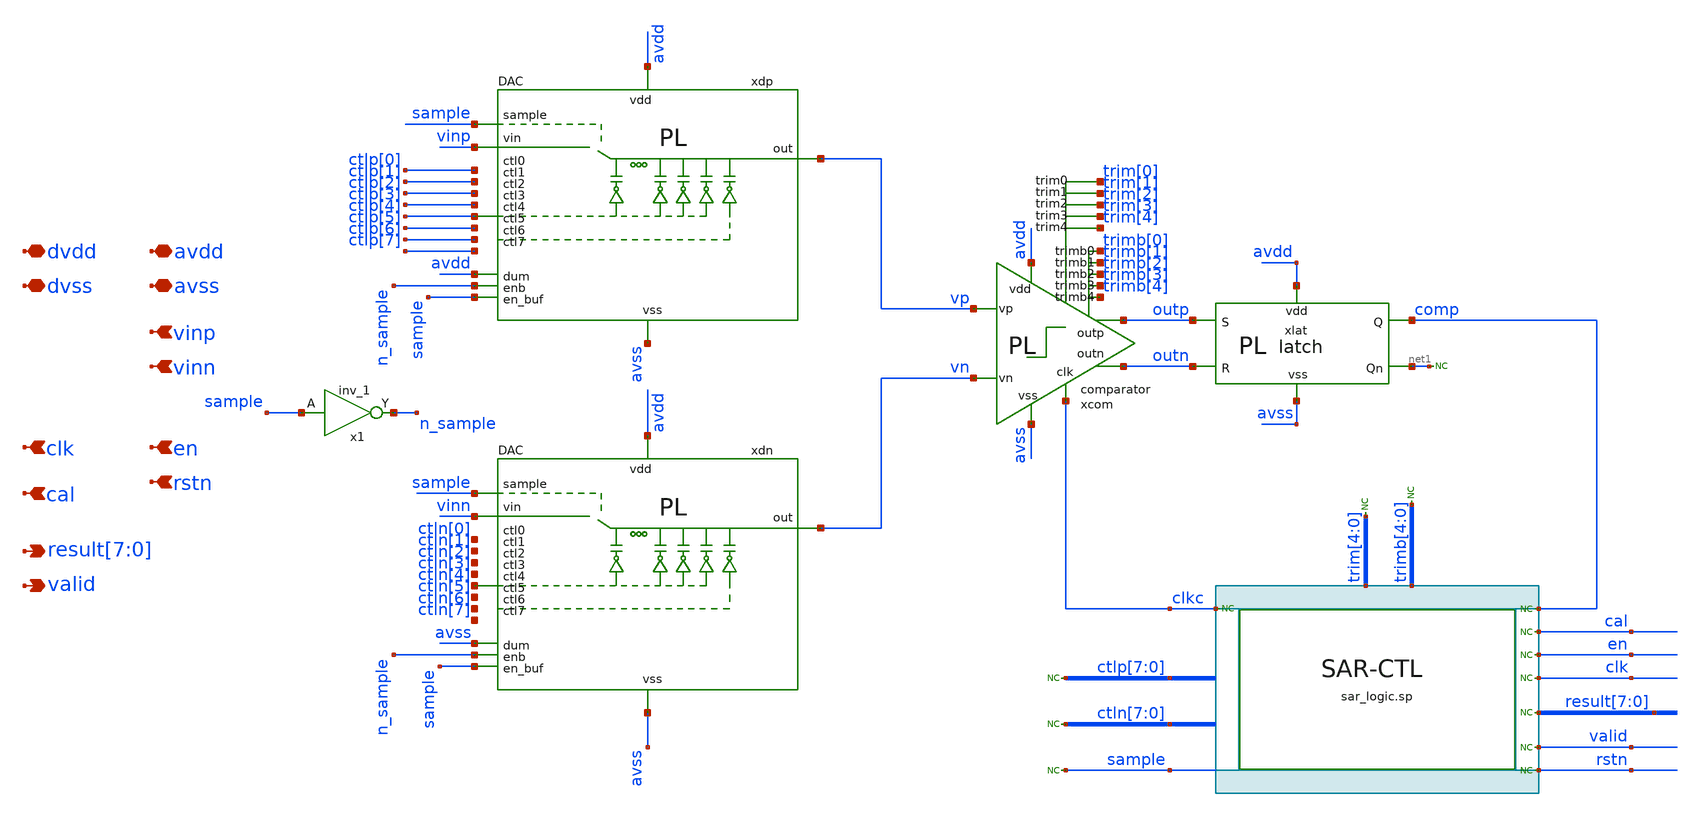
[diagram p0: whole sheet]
** sch_path: full_extract_sim/sar/sar_post/sar_post.sch
**.subckt sar_post avss avdd dvss dvdd vinp vinn
*+ result[7],result[6],result[5],result[4],result[3],result[2],result[1],result[0] clk en valid cal rstn
*.iopin avss
*.iopin avdd
*.iopin dvss
*.iopin dvdd
*.ipin vinp
*.ipin vinn
*.opin result[7],result[6],result[5],result[4],result[3],result[2],result[1],result[0]
*.ipin clk
*.ipin en
*.opin valid
*.ipin cal
*.ipin rstn
xlat avdd avss net1 outp outn comp latch
* noconn #net1
* noconn comp
* noconn sample
* noconn ctln[7:0]
* noconn ctlp[7:0]
* noconn trim[4:0]
* noconn trimb[4:0]
* noconn result[7:0]
* noconn valid
* noconn clkc
* noconn clk
* noconn en
* noconn cal
xdn n_sample sample ctln[1] ctln[0] avss ctln[3] ctln[4] ctln[5] ctln[6] ctln[7] ctln[2] avdd avss
+ sample vn vinn DAC
xcom trim[3] trim[2] trim[0] trim[1] trim[4] trimb[4] trimb[1] trimb[0] trimb[2] trimb[3] outn outp
+ clkc avdd avss vn vp comparator
* noconn rstn
xdp n_sample sample ctlp[1] ctlp[0] avdd ctlp[3] ctlp[4] ctlp[5] ctlp[6] ctlp[7] ctlp[2] avdd avss
+ sample vp vinp DAC
x1 sample VGND VNB VPB VPWR n_sample sky130_fd_sc_hd__inv_1
**** begin user architecture code


.model adc_buff adc_bridge(in_low = 0.2 in_high=0.8)
.model dac_buff dac_bridge(out_high = 1.2)

Aad [clk rstn en comp cal] [dclk drstn den dcomp dcal] adc_buff
Ada [dctlp0 dctlp1 dctlp2 dctlp3 dctlp4 dctlp5 dctlp6 dctlp7 dctln0 dctln1 dctln2 dctln3 dctln4
+ dctln5 dctln6 dctln7 dres0 dres1 dres2 dres3 dres4 dres5 dres6 dres7 dsamp dclkc] [ctlp_0_ ctlp_1_ ctlp_2_
+ ctlp_3_ ctlp_4_ ctlp_5_ ctlp_6_ ctlp_7_ ctln_0_ ctln_1_ ctln_2_ ctln_3_ ctln_4_ ctln_5_ ctln_6_ ctln_7_
+ res0 res1 res2 res3 res4 res5 res6 res7 sample clkc] dac_buff
Ada2 [dtrim4 dtrim3 dtrim2 dtrim1 dtrim0 dtrimb4 dtrimb3 dtrimb2 dtrimb1 dtrimb0] [trim_4_ trim_3_
+ trim_2_ trim_1_ trim_0_ trimb_4_ trimb_3_ trimb_2_ trimb_1_ trimb_0_ ] dac_buff

Xuut dvss dvdd dcal dclk dclkc dcomp dctln0 dctln1 dctln2 dctln3 dctln4 dctln5 dctln6 dctln7 dctlp0
+ dctlp1 dctlp2 dctlp3 dctlp4 dctlp5 dctlp6 dctlp7  den dres0 dres1 dres2 dres3 dres4 dres5 dres6 dres7
+ drstn dsamp dtrim0 dtrim1 dtrim2 dtrim3 dtrim4 dtrimb0 dtrimb1 dtrimb2 dtrimb3 dtrimb4 dvalid sar_logic



**** end user architecture code
**.ends
.end
